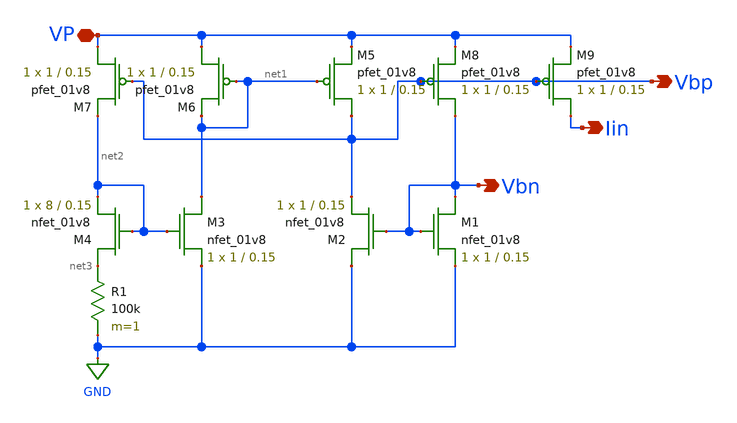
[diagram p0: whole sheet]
** sch_path: xschem/biasGen-j.sch
**.subckt biasGen-j Iin Vbp Vbn VP
*.opin Iin
*.opin Vbp
*.opin Vbn
*.iopin VP
XM1 Vbn Vbn GND GND sky130_fd_pr__nfet_01v8 L=0.15 W=1 nf=1 ad='int((nf+1)/2) * W/nf * 0.29' as='int((nf+2)/2) * W/nf * 0.29'
+ pd='2*int((nf+1)/2) * (W/nf + 0.29)' ps='2*int((nf+2)/2) * (W/nf + 0.29)' nrd='0.29 / W' nrs='0.29 / W'
+ sa=0 sb=0 sd=0 mult=1 m=1
XM2 GND Vbn Vbp GND sky130_fd_pr__nfet_01v8 L=0.15 W=1 nf=1 ad='int((nf+1)/2) * W/nf * 0.29' as='int((nf+2)/2) * W/nf * 0.29'
+ pd='2*int((nf+1)/2) * (W/nf + 0.29)' ps='2*int((nf+2)/2) * (W/nf + 0.29)' nrd='0.29 / W' nrs='0.29 / W'
+ sa=0 sb=0 sd=0 mult=1 m=1
XM3 net1 net2 GND GND sky130_fd_pr__nfet_01v8 L=0.15 W=1 nf=1 ad='int((nf+1)/2) * W/nf * 0.29' as='int((nf+2)/2) * W/nf * 0.29'
+ pd='2*int((nf+1)/2) * (W/nf + 0.29)' ps='2*int((nf+2)/2) * (W/nf + 0.29)' nrd='0.29 / W' nrs='0.29 / W'
+ sa=0 sb=0 sd=0 mult=1 m=1
XM4 net3 net2 net2 GND sky130_fd_pr__nfet_01v8 L=0.15 W=8 nf=1 ad='int((nf+1)/2) * W/nf * 0.29' as='int((nf+2)/2) * W/nf * 0.29'
+ pd='2*int((nf+1)/2) * (W/nf + 0.29)' ps='2*int((nf+2)/2) * (W/nf + 0.29)' nrd='0.29 / W' nrs='0.29 / W'
+ sa=0 sb=0 sd=0 mult=1 m=1
XM5 Vbp net1 VP VDD sky130_fd_pr__pfet_01v8 L=0.15 W=1 nf=1 ad='int((nf+1)/2) * W/nf * 0.29' as='int((nf+2)/2) * W/nf * 0.29'
+ pd='2*int((nf+1)/2) * (W/nf + 0.29)' ps='2*int((nf+2)/2) * (W/nf + 0.29)' nrd='0.29 / W' nrs='0.29 / W'
+ sa=0 sb=0 sd=0 mult=1 m=1
XM6 VP net1 net1 VDD sky130_fd_pr__pfet_01v8 L=0.15 W=1 nf=1 ad='int((nf+1)/2) * W/nf * 0.29' as='int((nf+2)/2) * W/nf * 0.29'
+ pd='2*int((nf+1)/2) * (W/nf + 0.29)' ps='2*int((nf+2)/2) * (W/nf + 0.29)' nrd='0.29 / W' nrs='0.29 / W'
+ sa=0 sb=0 sd=0 mult=1 m=1
XM7 VP Vbp net2 VDD sky130_fd_pr__pfet_01v8 L=0.15 W=1 nf=1 ad='int((nf+1)/2) * W/nf * 0.29' as='int((nf+2)/2) * W/nf * 0.29'
+ pd='2*int((nf+1)/2) * (W/nf + 0.29)' ps='2*int((nf+2)/2) * (W/nf + 0.29)' nrd='0.29 / W' nrs='0.29 / W'
+ sa=0 sb=0 sd=0 mult=1 m=1
XM8 Vbn Vbp VP VDD sky130_fd_pr__pfet_01v8 L=0.15 W=1 nf=1 ad='int((nf+1)/2) * W/nf * 0.29' as='int((nf+2)/2) * W/nf * 0.29'
+ pd='2*int((nf+1)/2) * (W/nf + 0.29)' ps='2*int((nf+2)/2) * (W/nf + 0.29)' nrd='0.29 / W' nrs='0.29 / W'
+ sa=0 sb=0 sd=0 mult=1 m=1
R1 net3 GND 100k m=1
XM9 Iin Vbp VP VDD sky130_fd_pr__pfet_01v8 L=0.15 W=1 nf=1 ad='int((nf+1)/2) * W/nf * 0.29' as='int((nf+2)/2) * W/nf * 0.29'
+ pd='2*int((nf+1)/2) * (W/nf + 0.29)' ps='2*int((nf+2)/2) * (W/nf + 0.29)' nrd='0.29 / W' nrs='0.29 / W'
+ sa=0 sb=0 sd=0 mult=1 m=1
**.ends
.GLOBAL GND
.end
